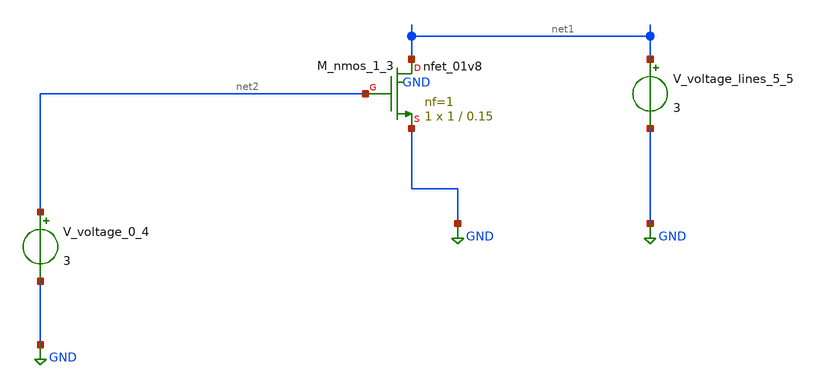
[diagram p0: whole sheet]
** sch_path: schematics/AMSNet/63.sch
**.subckt 63
XM_nmos_1_3 net1 net2 GND GND sky130_fd_pr__nfet_01v8 L=0.15 W=1 nf=1 ad='int((1 + 1)/2) * 1 / 1 * 0.29'
+ as='int((1 + 2)/2) * 1 / 1 * 0.29' pd='2*int((1 + 1)/2) * (1 / 1 + 0.29)' ps='2*int((1 + 2)/2) * (1 / 1 + 0.29)'
+ nrd='0.29 / 1 ' nrs='0.29 / 1 ' sa=0 sb=0 sd=0 mult=1 m=1
V_voltage_0_4 net2 GND 3
V_voltage_lines_5_5 net1 GND 3
**.ends
.GLOBAL GND
.end
